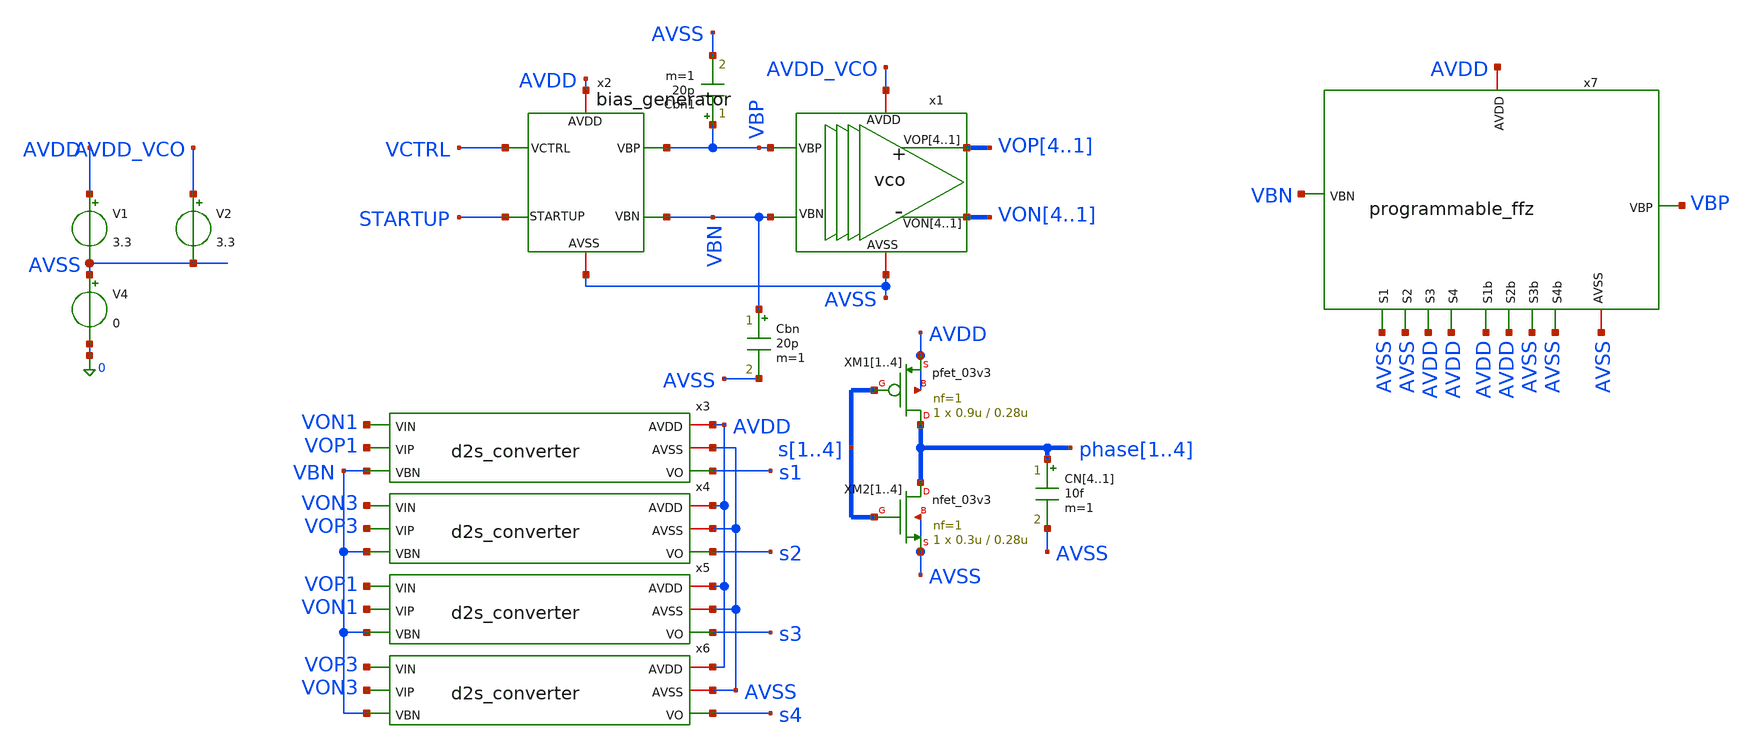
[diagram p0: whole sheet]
** sch_path: designs/libs/tb_analog/tb_quadrature_vco/tb_quadrature_vco.sch
**.subckt tb_quadrature_vco
x1 VOP4 VOP3 VOP2 VOP1 VON4 VON3 VON2 VON1 AVDD_VCO AVSS VBP VBN vco
V1 AVDD AVSS 3.3
V4 AVSS 0 0
CN4 phase1 AVSS 10f m=1
CN3 phase2 AVSS 10f m=1
CN2 phase3 AVSS 10f m=1
CN1 phase4 AVSS 10f m=1
x2 VCTRL AVDD STARTUP AVSS VBP VBN bias_generator
Cbn VBN AVSS 20p m=1
x3 AVDD AVSS VON1 VOP1 VBN s1 d2s_converter
XM11 phase1 s1 AVDD AVDD pfet_03v3 L=0.28u W=0.9u nf=1 ad='int((nf+1)/2) * W/nf * 0.18u' as='int((nf+2)/2) * W/nf * 0.18u'
+ pd='2*int((nf+1)/2) * (W/nf + 0.18u)' ps='2*int((nf+2)/2) * (W/nf + 0.18u)' nrd='0.18u / W' nrs='0.18u / W'
+ sa=0 sb=0 sd=0 m=1
XM12 phase2 s2 AVDD AVDD pfet_03v3 L=0.28u W=0.9u nf=1 ad='int((nf+1)/2) * W/nf * 0.18u' as='int((nf+2)/2) * W/nf * 0.18u'
+ pd='2*int((nf+1)/2) * (W/nf + 0.18u)' ps='2*int((nf+2)/2) * (W/nf + 0.18u)' nrd='0.18u / W' nrs='0.18u / W'
+ sa=0 sb=0 sd=0 m=1
XM13 phase3 s3 AVDD AVDD pfet_03v3 L=0.28u W=0.9u nf=1 ad='int((nf+1)/2) * W/nf * 0.18u' as='int((nf+2)/2) * W/nf * 0.18u'
+ pd='2*int((nf+1)/2) * (W/nf + 0.18u)' ps='2*int((nf+2)/2) * (W/nf + 0.18u)' nrd='0.18u / W' nrs='0.18u / W'
+ sa=0 sb=0 sd=0 m=1
XM14 phase4 s4 AVDD AVDD pfet_03v3 L=0.28u W=0.9u nf=1 ad='int((nf+1)/2) * W/nf * 0.18u' as='int((nf+2)/2) * W/nf * 0.18u'
+ pd='2*int((nf+1)/2) * (W/nf + 0.18u)' ps='2*int((nf+2)/2) * (W/nf + 0.18u)' nrd='0.18u / W' nrs='0.18u / W'
+ sa=0 sb=0 sd=0 m=1
XM21 phase1 s1 AVSS AVSS nfet_03v3 L=0.28u W=0.3u nf=1 ad='int((nf+1)/2) * W/nf * 0.18u' as='int((nf+2)/2) * W/nf * 0.18u'
+ pd='2*int((nf+1)/2) * (W/nf + 0.18u)' ps='2*int((nf+2)/2) * (W/nf + 0.18u)' nrd='0.18u / W' nrs='0.18u / W'
+ sa=0 sb=0 sd=0 m=1
XM22 phase2 s2 AVSS AVSS nfet_03v3 L=0.28u W=0.3u nf=1 ad='int((nf+1)/2) * W/nf * 0.18u' as='int((nf+2)/2) * W/nf * 0.18u'
+ pd='2*int((nf+1)/2) * (W/nf + 0.18u)' ps='2*int((nf+2)/2) * (W/nf + 0.18u)' nrd='0.18u / W' nrs='0.18u / W'
+ sa=0 sb=0 sd=0 m=1
XM23 phase3 s3 AVSS AVSS nfet_03v3 L=0.28u W=0.3u nf=1 ad='int((nf+1)/2) * W/nf * 0.18u' as='int((nf+2)/2) * W/nf * 0.18u'
+ pd='2*int((nf+1)/2) * (W/nf + 0.18u)' ps='2*int((nf+2)/2) * (W/nf + 0.18u)' nrd='0.18u / W' nrs='0.18u / W'
+ sa=0 sb=0 sd=0 m=1
XM24 phase4 s4 AVSS AVSS nfet_03v3 L=0.28u W=0.3u nf=1 ad='int((nf+1)/2) * W/nf * 0.18u' as='int((nf+2)/2) * W/nf * 0.18u'
+ pd='2*int((nf+1)/2) * (W/nf + 0.18u)' ps='2*int((nf+2)/2) * (W/nf + 0.18u)' nrd='0.18u / W' nrs='0.18u / W'
+ sa=0 sb=0 sd=0 m=1
x4 AVDD AVSS VON3 VOP3 VBN s2 d2s_converter
x5 AVDD AVSS VOP1 VON1 VBN s3 d2s_converter
x6 AVDD AVSS VOP3 VON3 VBN s4 d2s_converter
V2 AVDD_VCO AVSS 3.3
Cbn1 VBP AVSS 20p m=1
x7 VBP AVSS AVDD VBN AVDD AVSS AVDD AVSS AVSS AVDD AVSS AVDD programmable_ffz
**** begin user architecture code


.param Vin=0 Vcm=2.5
.ic v(vop1)=3.3 v(von1)=0 v(startup)=0 v(vbp)=0
.param t1=1u t2=2u t3=3u t4=4u t5=5u t6=6u t7=10u t8=100u t9=1m tr=10n

.param d0=0 d1=0.35 d2=0.825 d3=1.2375 d4=1.65 d5=2.0625 d6=2.475 d7=2.6 d8=2.75

vs startup 0 pulse(0 1 100n 10n 10n 100n 100m)
vctrl vctrl 0 pwl(0 d0  t1 d0 't1+tr' d1 t2 d1 't2+tr' d2 t3 d2 't3+tr' d3 t4 d3 't4+tr' d4 t5 d4 't5+tr'
+ d5 t6 d5 't6+tr' d6 t7 d6 't7+tr' d7 t8 d7 't8+tr' d8 t9 d8 't9+tr' d0 R 0)

*vctrl vctrl 0 1

.control
set wr_singlescale
set wr_vecnames

save v(phase1) v(phase2) v(phase3) v(phase4) v(vctrl) v(vbp) v(vbn)

OP
show all

tran 1n 1.5m
*tran 10p 10u 0 1p
*DC V5 -1 1 0.01

*let sum = v(VOP1) + v(VON1)
*let diff = v(VOP1) - v(VON1)
*let gain = deriv(diff)
*let vcm = AVG(sum/2)


*meas tran vmax MAX v(VOP1) FROM=10n TO=20n
*meas tran vmin MIN v(VOP1) FROM=10n TO=20n
*let vswing = vmax-vmin

*meas tran I_tail_avg1 AVG i(v.x1.x1.vmeas) FROM=1.01u TO=2u
*meas tran I_tail_avg2 AVG i(v.x1.x1.vmeas) FROM=2.01u TO=3u
*meas tran I_tail_avg3 AVG i(v.x1.x1.vmeas) FROM=3.01u TO=4u
*meas tran I_tail_avg4 AVG i(v.x1.x1.vmeas) FROM=4.01u TO=5u
*meas tran I_tail_avg5 AVG i(v.x1.x1.vmeas) FROM=5.01u TO=6u
*meas tran I_tail_avg6 AVG i(v.x1.x1.vmeas) FROM=6.01u TO=10u
*meas tran I_tail_avg7 AVG i(v.x1.x1.vmeas) FROM=10.01u TO=100u
*meas tran I_tail_avg8 AVG i(v.x1.x1.vmeas) FROM=100.01u TO=1m

*meas tran I_VCO1 AVG i(V2) FROM=1.01u TO=2u
*meas tran I_VCO2 AVG i(V2) FROM=2.01u TO=3u
*meas tran I_VCO3 AVG i(V2) FROM=3.01u TO=4u
*meas tran I_VCO4 AVG i(V2) FROM=4.01u TO=5u
*meas tran I_VCO5 AVG i(V2) FROM=5.01u TO=6u
*meas tran I_VCO6 AVG i(V2) FROM=6.01u TO=10u
*meas tran I_VCO7 AVG i(V2) FROM=10.01u TO=100u
*meas tran I_VCO8 AVG i(V2) FROM=100.01u TO=1m

remzerovec

write tb_quadrature_vco.raw
*wrdata /foss/designs/synchronos-chipathon-2026/designs/libs/scripts/sim_data/tb_quadrature_vco.txt
*+ tran.all
.endc



.include $::180MCU_MODELS/design.ngspice
.lib $::180MCU_MODELS/sm141064.ngspice typical
*.lib $::180MCU_MODELS/sm141064.ngspice SS
*.lib $::180MCU_MODELS/sm141064.ngspice FF
*.lib $::180MCU_MODELS/sm141064.ngspice SF
*.lib $::180MCU_MODELS/sm141064.ngspice FS

**** end user architecture code
**.ends

* expanding   symbol:  libs/core_analog/vco/vco.sym # of pins=6
** sym_path: designs/libs/core_analog/vco/vco.sym
** sch_path: designs/libs/core_analog/vco/vco.sch
.subckt vco VOP4 VOP3 VOP2 VOP1 VON4 VON3 VON2 VON1 AVDD AVSS VBP VBN
*.opin VOP1,VOP2,VOP3,VOP4
*.opin VON1,VON2,VON3,VON4
*.ipin VBP
*.ipin VBN
*.iopin AVDD
*.iopin AVSS
x1 VOP1 AVDD VOP4 VON4 VON1 AVSS VBP VBN delay_stage
x2 VOP2 AVDD VON1 VOP1 VON2 AVSS VBP VBN delay_stage
x3 VOP3 AVDD VON2 VOP2 VON3 AVSS VBP VBN delay_stage
x4 VOP4 AVDD VON3 VOP3 VON4 AVSS VBP VBN delay_stage
.ends


* expanding   symbol:  libs/core_analog/bias_generator/bias_generator.sym # of pins=6
** sym_path: designs/libs/core_analog/bias_generator/bias_generator.sym
** sch_path: designs/libs/core_analog/bias_generator/bias_generator.sch
.subckt bias_generator VCTRL AVDD STARTUP AVSS VBP VBN
*.ipin VCTRL
*.ipin STARTUP
*.iopin AVDD
*.iopin AVSS
*.opin VBP
*.opin VBN
x1 VBN AVDD net2 VCTRL AVSS net1 ota_5t
Vmeas net6 net3 0
.save i(vmeas)
Vmeas1 net7 net5 0
.save i(vmeas1)
Vmeas2 net8 net4 0
.save i(vmeas2)
XM1 net1 net1 AVDD AVDD pfet_03v3 L=0.5u W=16.8u nf=1 ad='int((nf+1)/2) * W/nf * 0.18u' as='int((nf+2)/2) * W/nf * 0.18u'
+ pd='2*int((nf+1)/2) * (W/nf + 0.18u)' ps='2*int((nf+2)/2) * (W/nf + 0.18u)' nrd='0.18u / W' nrs='0.18u / W'
+ sa=0 sb=0 sd=0 m=16
XM8 net2 AVDD net7 AVSS nfet_03v3 L=0.5u W=2.08u nf=1 ad='int((nf+1)/2) * W/nf * 0.18u' as='int((nf+2)/2) * W/nf * 0.18u'
+ pd='2*int((nf+1)/2) * (W/nf + 0.18u)' ps='2*int((nf+2)/2) * (W/nf + 0.18u)' nrd='0.18u / W' nrs='0.18u / W'
+ sa=0 sb=0 sd=0 m=8
XM9 VBP AVDD net8 AVSS nfet_03v3 L=0.5u W=2.08u nf=1 ad='int((nf+1)/2) * W/nf * 0.18u' as='int((nf+2)/2) * W/nf * 0.18u'
+ pd='2*int((nf+1)/2) * (W/nf + 0.18u)' ps='2*int((nf+2)/2) * (W/nf + 0.18u)' nrd='0.18u / W' nrs='0.18u / W'
+ sa=0 sb=0 sd=0 m=56
XM11 net1 AVDD net6 AVSS nfet_03v3 L=0.5u W=2.08u nf=1 ad='int((nf+1)/2) * W/nf * 0.18u' as='int((nf+2)/2) * W/nf * 0.18u'
+ pd='2*int((nf+1)/2) * (W/nf + 0.18u)' ps='2*int((nf+2)/2) * (W/nf + 0.18u)' nrd='0.18u / W' nrs='0.18u / W'
+ sa=0 sb=0 sd=0 m=8
XM12 net4 VBN AVSS AVSS nfet_03v3 L=0.5u W=11.25u nf=1 ad='int((nf+1)/2) * W/nf * 0.18u' as='int((nf+2)/2) * W/nf * 0.18u'
+ pd='2*int((nf+1)/2) * (W/nf + 0.18u)' ps='2*int((nf+2)/2) * (W/nf + 0.18u)' nrd='0.18u / W' nrs='0.18u / W'
+ sa=0 sb=0 sd=0 m=56
XM3 net5 VBN AVSS AVSS nfet_03v3 L=0.5u W=11.25u nf=1 ad='int((nf+1)/2) * W/nf * 0.18u' as='int((nf+2)/2) * W/nf * 0.18u'
+ pd='2*int((nf+1)/2) * (W/nf + 0.18u)' ps='2*int((nf+2)/2) * (W/nf + 0.18u)' nrd='0.18u / W' nrs='0.18u / W'
+ sa=0 sb=0 sd=0 m=8
XM4 net3 VBN AVSS AVSS nfet_03v3 L=0.5u W=11.25u nf=1 ad='int((nf+1)/2) * W/nf * 0.18u' as='int((nf+2)/2) * W/nf * 0.18u'
+ pd='2*int((nf+1)/2) * (W/nf + 0.18u)' ps='2*int((nf+2)/2) * (W/nf + 0.18u)' nrd='0.18u / W' nrs='0.18u / W'
+ sa=0 sb=0 sd=0 m=8
XM10 net3 STARTUP AVSS AVSS nfet_03v3 L=0.5u W=11.25u nf=1 ad='int((nf+1)/2) * W/nf * 0.18u' as='int((nf+2)/2) * W/nf * 0.18u'
+ pd='2*int((nf+1)/2) * (W/nf + 0.18u)' ps='2*int((nf+2)/2) * (W/nf + 0.18u)' nrd='0.18u / W' nrs='0.18u / W'
+ sa=0 sb=0 sd=0 m=8
XM2 net2 VCTRL AVDD AVDD pfet_03v3 L=1.5u W=1.1u nf=1 ad='int((nf+1)/2) * W/nf * 0.18u' as='int((nf+2)/2) * W/nf * 0.18u'
+ pd='2*int((nf+1)/2) * (W/nf + 0.18u)' ps='2*int((nf+2)/2) * (W/nf + 0.18u)' nrd='0.18u / W' nrs='0.18u / W'
+ sa=0 sb=0 sd=0 m=8
XM5 net2 net2 AVDD AVDD pfet_03v3 L=1.5u W=1.1u nf=1 ad='int((nf+1)/2) * W/nf * 0.18u' as='int((nf+2)/2) * W/nf * 0.18u'
+ pd='2*int((nf+1)/2) * (W/nf + 0.18u)' ps='2*int((nf+2)/2) * (W/nf + 0.18u)' nrd='0.18u / W' nrs='0.18u / W'
+ sa=0 sb=0 sd=0 m=8
XM6 VBP VBP AVDD AVDD pfet_03v3 L=1.5u W=1.1u nf=1 ad='int((nf+1)/2) * W/nf * 0.18u' as='int((nf+2)/2) * W/nf * 0.18u'
+ pd='2*int((nf+1)/2) * (W/nf + 0.18u)' ps='2*int((nf+2)/2) * (W/nf + 0.18u)' nrd='0.18u / W' nrs='0.18u / W'
+ sa=0 sb=0 sd=0 m=56
XM7 VBP VBP AVDD AVDD pfet_03v3 L=1.5u W=1.1u nf=1 ad='int((nf+1)/2) * W/nf * 0.18u' as='int((nf+2)/2) * W/nf * 0.18u'
+ pd='2*int((nf+1)/2) * (W/nf + 0.18u)' ps='2*int((nf+2)/2) * (W/nf + 0.18u)' nrd='0.18u / W' nrs='0.18u / W'
+ sa=0 sb=0 sd=0 m=56
.ends


* expanding   symbol:  libs/core_analog/d2s_converter/d2s_converter.sym # of pins=6
** sym_path: designs/libs/core_analog/d2s_converter/d2s_converter.sym
** sch_path: designs/libs/core_analog/d2s_converter/d2s_converter.sch
.subckt d2s_converter AVDD AVSS VIN VIP VBN VO
*.iopin AVDD
*.iopin AVSS
*.ipin VIN
*.ipin VIP
*.opin VO
*.ipin VBN
XM2 VOPB VIN i1 AVSS nfet_03v3 L=0.3u W=1.9u nf=1 ad='int((nf+1)/2) * W/nf * 0.18u' as='int((nf+2)/2) * W/nf * 0.18u'
+ pd='2*int((nf+1)/2) * (W/nf + 0.18u)' ps='2*int((nf+2)/2) * (W/nf + 0.18u)' nrd='0.18u / W' nrs='0.18u / W'
+ sa=0 sb=0 sd=0 m=4
XM4 VOPB VOPB AVDD AVDD pfet_03v3 L=0.3u W=1.4u nf=1 ad='int((nf+1)/2) * W/nf * 0.18u' as='int((nf+2)/2) * W/nf * 0.18u'
+ pd='2*int((nf+1)/2) * (W/nf + 0.18u)' ps='2*int((nf+2)/2) * (W/nf + 0.18u)' nrd='0.18u / W' nrs='0.18u / W'
+ sa=0 sb=0 sd=0 m=4
XM11 VOB VOB AVSS AVSS nfet_03v3 L=0.3u W=1.5u nf=1 ad='int((nf+1)/2) * W/nf * 0.18u' as='int((nf+2)/2) * W/nf * 0.18u'
+ pd='2*int((nf+1)/2) * (W/nf + 0.18u)' ps='2*int((nf+2)/2) * (W/nf + 0.18u)' nrd='0.18u / W' nrs='0.18u / W'
+ sa=0 sb=0 sd=0 m=4
XM13 VOB VOP AVDD AVDD pfet_03v3 L=0.3u W=2u nf=1 ad='int((nf+1)/2) * W/nf * 0.18u' as='int((nf+2)/2) * W/nf * 0.18u'
+ pd='2*int((nf+1)/2) * (W/nf + 0.18u)' ps='2*int((nf+2)/2) * (W/nf + 0.18u)' nrd='0.18u / W' nrs='0.18u / W'
+ sa=0 sb=0 sd=0 m=4
XM3 VOP VIP i1 AVSS nfet_03v3 L=0.3u W=1.9u nf=1 ad='int((nf+1)/2) * W/nf * 0.18u' as='int((nf+2)/2) * W/nf * 0.18u'
+ pd='2*int((nf+1)/2) * (W/nf + 0.18u)' ps='2*int((nf+2)/2) * (W/nf + 0.18u)' nrd='0.18u / W' nrs='0.18u / W'
+ sa=0 sb=0 sd=0 m=4
XM5 VOP VOPB AVDD AVDD pfet_03v3 L=0.3u W=1.4u nf=1 ad='int((nf+1)/2) * W/nf * 0.18u' as='int((nf+2)/2) * W/nf * 0.18u'
+ pd='2*int((nf+1)/2) * (W/nf + 0.18u)' ps='2*int((nf+2)/2) * (W/nf + 0.18u)' nrd='0.18u / W' nrs='0.18u / W'
+ sa=0 sb=0 sd=0 m=4
XM7 VONB VIP i2 AVSS nfet_03v3 L=0.3u W=1.9u nf=1 ad='int((nf+1)/2) * W/nf * 0.18u' as='int((nf+2)/2) * W/nf * 0.18u'
+ pd='2*int((nf+1)/2) * (W/nf + 0.18u)' ps='2*int((nf+2)/2) * (W/nf + 0.18u)' nrd='0.18u / W' nrs='0.18u / W'
+ sa=0 sb=0 sd=0 m=4
XM8 VONB VONB AVDD AVDD pfet_03v3 L=0.3u W=1.4u nf=1 ad='int((nf+1)/2) * W/nf * 0.18u' as='int((nf+2)/2) * W/nf * 0.18u'
+ pd='2*int((nf+1)/2) * (W/nf + 0.18u)' ps='2*int((nf+2)/2) * (W/nf + 0.18u)' nrd='0.18u / W' nrs='0.18u / W'
+ sa=0 sb=0 sd=0 m=4
XM9 VON VIN i2 AVSS nfet_03v3 L=0.3u W=1.9u nf=1 ad='int((nf+1)/2) * W/nf * 0.18u' as='int((nf+2)/2) * W/nf * 0.18u'
+ pd='2*int((nf+1)/2) * (W/nf + 0.18u)' ps='2*int((nf+2)/2) * (W/nf + 0.18u)' nrd='0.18u / W' nrs='0.18u / W'
+ sa=0 sb=0 sd=0 m=4
XM10 VON VONB AVDD AVDD pfet_03v3 L=0.3u W=1.4u nf=1 ad='int((nf+1)/2) * W/nf * 0.18u' as='int((nf+2)/2) * W/nf * 0.18u'
+ pd='2*int((nf+1)/2) * (W/nf + 0.18u)' ps='2*int((nf+2)/2) * (W/nf + 0.18u)' nrd='0.18u / W' nrs='0.18u / W'
+ sa=0 sb=0 sd=0 m=4
XM14 VO VON AVDD AVDD pfet_03v3 L=0.3u W=2u nf=1 ad='int((nf+1)/2) * W/nf * 0.18u' as='int((nf+2)/2) * W/nf * 0.18u'
+ pd='2*int((nf+1)/2) * (W/nf + 0.18u)' ps='2*int((nf+2)/2) * (W/nf + 0.18u)' nrd='0.18u / W' nrs='0.18u / W'
+ sa=0 sb=0 sd=0 m=4
XM12 VO VOB AVSS AVSS nfet_03v3 L=0.3u W=1.5u nf=1 ad='int((nf+1)/2) * W/nf * 0.18u' as='int((nf+2)/2) * W/nf * 0.18u'
+ pd='2*int((nf+1)/2) * (W/nf + 0.18u)' ps='2*int((nf+2)/2) * (W/nf + 0.18u)' nrd='0.18u / W' nrs='0.18u / W'
+ sa=0 sb=0 sd=0 m=4
XM1 i1 VBN AVSS AVSS nfet_03v3 L=0.5u W=11.25u nf=1 ad='int((nf+1)/2) * W/nf * 0.18u' as='int((nf+2)/2) * W/nf * 0.18u'
+ pd='2*int((nf+1)/2) * (W/nf + 0.18u)' ps='2*int((nf+2)/2) * (W/nf + 0.18u)' nrd='0.18u / W' nrs='0.18u / W'
+ sa=0 sb=0 sd=0 m=4
XM6 i2 VBN AVSS AVSS nfet_03v3 L=0.5u W=11.25u nf=1 ad='int((nf+1)/2) * W/nf * 0.18u' as='int((nf+2)/2) * W/nf * 0.18u'
+ pd='2*int((nf+1)/2) * (W/nf + 0.18u)' ps='2*int((nf+2)/2) * (W/nf + 0.18u)' nrd='0.18u / W' nrs='0.18u / W'
+ sa=0 sb=0 sd=0 m=4
.ends


* expanding   symbol:  libs/core_analog/programmable_ffz/programmable_ffz.sym # of pins=12
** sym_path: designs/libs/core_analog/programmable_ffz/programmable_ffz.sym
** sch_path: designs/libs/core_analog/programmable_ffz/programmable_ffz.sch
.subckt programmable_ffz VBP AVSS AVDD VBN S1b S1 S2b S2 S3b S3 S4b S4
*.ipin VBN
*.ipin S1b
*.ipin S1
*.ipin S2b
*.ipin S2
*.ipin S3b
*.ipin S3
*.ipin S4b
*.ipin S4
*.iopin AVSS
*.iopin AVDD
*.opin VBP
x2 VBN AVSS S1 VBN1 S1b AVDD transmission_gate
x3 VBN AVSS S2 VBN2 S2b AVDD transmission_gate
x4 VBN AVSS S3 VBN3 S3b AVDD transmission_gate
x5 VBN AVSS S4 VBN4 S4b AVDD transmission_gate
x1 AVDD VBP VBN AVSS AVSS feed_forward_zero
x6 AVDD net1 VBN1 S1b AVSS feed_forward_zero
x71 AVDD net2 VBN2 S2b AVSS feed_forward_zero
x72 AVDD net2 VBN2 S2b AVSS feed_forward_zero
x11 AVDD net3 VBN3 S3b AVSS feed_forward_zero
x12 AVDD net3 VBN3 S3b AVSS feed_forward_zero
x13 AVDD net3 VBN3 S3b AVSS feed_forward_zero
x14 AVDD net3 VBN3 S3b AVSS feed_forward_zero
x21 AVDD net4 VBN4 S4b AVSS feed_forward_zero
x22 AVDD net4 VBN4 S4b AVSS feed_forward_zero
x23 AVDD net4 VBN4 S4b AVSS feed_forward_zero
x24 AVDD net4 VBN4 S4b AVSS feed_forward_zero
x25 AVDD net4 VBN4 S4b AVSS feed_forward_zero
x26 AVDD net4 VBN4 S4b AVSS feed_forward_zero
x27 AVDD net4 VBN4 S4b AVSS feed_forward_zero
x28 AVDD net4 VBN4 S4b AVSS feed_forward_zero
x7 net1 AVSS S1 VBP S1b AVDD transmission_gate
x8 net2 AVSS S2 VBP S2b AVDD transmission_gate
x9 net3 AVSS S3 VBP S3b AVDD transmission_gate
x10 net4 AVSS S4 VBP S4b AVDD transmission_gate
.ends


* expanding   symbol:  libs/core_analog/delay_stage/delay_stage.sym # of pins=8
** sym_path: designs/libs/core_analog/delay_stage/delay_stage.sym
** sch_path: designs/libs/core_analog/delay_stage/delay_stage.sch
.subckt delay_stage VOP AVDD VIP VIN VON AVSS VBP VBN
*.ipin VIP
*.ipin VIN
*.opin VOP
*.opin VON
*.iopin AVDD
*.iopin AVSS
*.ipin VBP
*.ipin VBN
XM5 VON VIP net1 AVSS nfet_03v3 L=0.5u W=2.08u nf=1 ad='int((nf+1)/2) * W/nf * 0.18u' as='int((nf+2)/2) * W/nf * 0.18u'
+ pd='2*int((nf+1)/2) * (W/nf + 0.18u)' ps='2*int((nf+2)/2) * (W/nf + 0.18u)' nrd='0.18u / W' nrs='0.18u / W'
+ sa=0 sb=0 sd=0 m=8
XM2 VON VON AVDD AVDD pfet_03v3 L=1.5u W=1.1u nf=1 ad='int((nf+1)/2) * W/nf * 0.18u' as='int((nf+2)/2) * W/nf * 0.18u'
+ pd='2*int((nf+1)/2) * (W/nf + 0.18u)' ps='2*int((nf+2)/2) * (W/nf + 0.18u)' nrd='0.18u / W' nrs='0.18u / W'
+ sa=0 sb=0 sd=0 m=8
XM6 VOP VIN net1 AVSS nfet_03v3 L=0.5u W=2.08u nf=1 ad='int((nf+1)/2) * W/nf * 0.18u' as='int((nf+2)/2) * W/nf * 0.18u'
+ pd='2*int((nf+1)/2) * (W/nf + 0.18u)' ps='2*int((nf+2)/2) * (W/nf + 0.18u)' nrd='0.18u / W' nrs='0.18u / W'
+ sa=0 sb=0 sd=0 m=8
XM1 VON VBP AVDD AVDD pfet_03v3 L=1.5u W=1.1u nf=1 ad='int((nf+1)/2) * W/nf * 0.18u' as='int((nf+2)/2) * W/nf * 0.18u'
+ pd='2*int((nf+1)/2) * (W/nf + 0.18u)' ps='2*int((nf+2)/2) * (W/nf + 0.18u)' nrd='0.18u / W' nrs='0.18u / W'
+ sa=0 sb=0 sd=0 m=8
XM3 VOP VBP AVDD AVDD pfet_03v3 L=1.5u W=1.1u nf=1 ad='int((nf+1)/2) * W/nf * 0.18u' as='int((nf+2)/2) * W/nf * 0.18u'
+ pd='2*int((nf+1)/2) * (W/nf + 0.18u)' ps='2*int((nf+2)/2) * (W/nf + 0.18u)' nrd='0.18u / W' nrs='0.18u / W'
+ sa=0 sb=0 sd=0 m=8
XM4 VOP VOP AVDD AVDD pfet_03v3 L=1.5u W=1.1u nf=1 ad='int((nf+1)/2) * W/nf * 0.18u' as='int((nf+2)/2) * W/nf * 0.18u'
+ pd='2*int((nf+1)/2) * (W/nf + 0.18u)' ps='2*int((nf+2)/2) * (W/nf + 0.18u)' nrd='0.18u / W' nrs='0.18u / W'
+ sa=0 sb=0 sd=0 m=8
XM8 net1 VBN AVSS AVSS nfet_03v3 L=0.5u W=11.25u nf=1 ad='int((nf+1)/2) * W/nf * 0.18u' as='int((nf+2)/2) * W/nf * 0.18u'
+ pd='2*int((nf+1)/2) * (W/nf + 0.18u)' ps='2*int((nf+2)/2) * (W/nf + 0.18u)' nrd='0.18u / W' nrs='0.18u / W'
+ sa=0 sb=0 sd=0 m=8
.ends


* expanding   symbol:  libs/core_analog/ota_5t/ota_5t.sym # of pins=6
** sym_path: designs/libs/core_analog/ota_5t/ota_5t.sym
** sch_path: designs/libs/core_analog/ota_5t/ota_5t.sch
.subckt ota_5t VO AVDD VI+ VI- AVSS VB
*.ipin VI+
*.ipin VI-
*.ipin VB
*.iopin AVDD
*.iopin AVSS
*.opin VO
XM1 VO VI- net2 AVDD pfet_03v3 L=0.5u W=6.55u nf=1 ad='int((nf+1)/2) * W/nf * 0.18u' as='int((nf+2)/2) * W/nf * 0.18u'
+ pd='2*int((nf+1)/2) * (W/nf + 0.18u)' ps='2*int((nf+2)/2) * (W/nf + 0.18u)' nrd='0.18u / W' nrs='0.18u / W'
+ sa=0 sb=0 sd=0 m=8
XM4 VO net1 AVSS AVSS nfet_03v3 L=0.5u W=4.8u nf=1 ad='int((nf+1)/2) * W/nf * 0.18u' as='int((nf+2)/2) * W/nf * 0.18u'
+ pd='2*int((nf+1)/2) * (W/nf + 0.18u)' ps='2*int((nf+2)/2) * (W/nf + 0.18u)' nrd='0.18u / W' nrs='0.18u / W'
+ sa=0 sb=0 sd=0 m=4
XM3 net2 VB net3 AVDD pfet_03v3 L=0.5u W=8.3u nf=1 ad='int((nf+1)/2) * W/nf * 0.18u' as='int((nf+2)/2) * W/nf * 0.18u'
+ pd='2*int((nf+1)/2) * (W/nf + 0.18u)' ps='2*int((nf+2)/2) * (W/nf + 0.18u)' nrd='0.18u / W' nrs='0.18u / W'
+ sa=0 sb=0 sd=0 m=16
XM2 net1 VI+ net2 AVDD pfet_03v3 L=0.5u W=6.55u nf=1 ad='int((nf+1)/2) * W/nf * 0.18u' as='int((nf+2)/2) * W/nf * 0.18u'
+ pd='2*int((nf+1)/2) * (W/nf + 0.18u)' ps='2*int((nf+2)/2) * (W/nf + 0.18u)' nrd='0.18u / W' nrs='0.18u / W'
+ sa=0 sb=0 sd=0 m=8
XM5 net1 net1 AVSS AVSS nfet_03v3 L=0.5u W=4.8u nf=1 ad='int((nf+1)/2) * W/nf * 0.18u' as='int((nf+2)/2) * W/nf * 0.18u'
+ pd='2*int((nf+1)/2) * (W/nf + 0.18u)' ps='2*int((nf+2)/2) * (W/nf + 0.18u)' nrd='0.18u / W' nrs='0.18u / W'
+ sa=0 sb=0 sd=0 m=4
Vmeas AVDD net3 0
.save i(vmeas)
.ends


* expanding   symbol:  libs/core_analog/transmission_gate/transmission_gate.sym # of pins=6
** sym_path: designs/libs/core_analog/transmission_gate/transmission_gate.sym
** sch_path: designs/libs/core_analog/transmission_gate/transmission_gate.sch
.subckt transmission_gate ind vss clkn ins clkp vdd
*.iopin ind
*.iopin ins
*.iopin clkn
*.iopin clkp
*.iopin vdd
*.iopin vss
XM1 ind clkp ins vdd pfet_03v3 L=0.5u W=3.0u nf=1 ad='int((nf+1)/2) * W/nf * 0.18u' as='int((nf+2)/2) * W/nf * 0.18u'
+ pd='2*int((nf+1)/2) * (W/nf + 0.18u)' ps='2*int((nf+2)/2) * (W/nf + 0.18u)' nrd='0.18u / W' nrs='0.18u / W'
+ sa=0 sb=0 sd=0 m=1
XM2 ind clkn ins vss nfet_03v3 L=0.5u W=1.0u nf=1 ad='int((nf+1)/2) * W/nf * 0.18u' as='int((nf+2)/2) * W/nf * 0.18u'
+ pd='2*int((nf+1)/2) * (W/nf + 0.18u)' ps='2*int((nf+2)/2) * (W/nf + 0.18u)' nrd='0.18u / W' nrs='0.18u / W'
+ sa=0 sb=0 sd=0 m=1
.ends


* expanding   symbol:  libs/core_analog/feed_forward_zero/feed_forward_zero.sym # of pins=5
** sym_path: designs/libs/core_analog/feed_forward_zero/feed_forward_zero.sym
** sch_path: designs/libs/core_analog/feed_forward_zero/feed_forward_zero.sch
.subckt feed_forward_zero AVDD VBP VBN S AVSS
*.opin VBP
*.iopin AVDD
*.iopin AVSS
*.ipin VBN
*.ipin S
XM1 VBP VBP AVDD AVDD pfet_03v3 L=1.5u W=1.1u nf=1 ad='int((nf+1)/2) * W/nf * 0.18u' as='int((nf+2)/2) * W/nf * 0.18u'
+ pd='2*int((nf+1)/2) * (W/nf + 0.18u)' ps='2*int((nf+2)/2) * (W/nf + 0.18u)' nrd='0.18u / W' nrs='0.18u / W'
+ sa=0 sb=0 sd=0 m=2
XM2 VBP VBP AVDD AVDD pfet_03v3 L=1.5u W=1.1u nf=1 ad='int((nf+1)/2) * W/nf * 0.18u' as='int((nf+2)/2) * W/nf * 0.18u'
+ pd='2*int((nf+1)/2) * (W/nf + 0.18u)' ps='2*int((nf+2)/2) * (W/nf + 0.18u)' nrd='0.18u / W' nrs='0.18u / W'
+ sa=0 sb=0 sd=0 m=2
XM3 VBP AVDD net1 AVSS nfet_03v3 L=0.5u W=2.08u nf=1 ad='int((nf+1)/2) * W/nf * 0.18u' as='int((nf+2)/2) * W/nf * 0.18u'
+ pd='2*int((nf+1)/2) * (W/nf + 0.18u)' ps='2*int((nf+2)/2) * (W/nf + 0.18u)' nrd='0.18u / W' nrs='0.18u / W'
+ sa=0 sb=0 sd=0 m=2
XM4 net1 VBN AVSS AVSS nfet_03v3 L=0.5u W=11.25u nf=1 ad='int((nf+1)/2) * W/nf * 0.18u' as='int((nf+2)/2) * W/nf * 0.18u'
+ pd='2*int((nf+1)/2) * (W/nf + 0.18u)' ps='2*int((nf+2)/2) * (W/nf + 0.18u)' nrd='0.18u / W' nrs='0.18u / W'
+ sa=0 sb=0 sd=0 m=2
XM7 VBN S AVSS AVSS nfet_03v3 L=0.5u W=1u nf=1 ad='int((nf+1)/2) * W/nf * 0.18u' as='int((nf+2)/2) * W/nf * 0.18u'
+ pd='2*int((nf+1)/2) * (W/nf + 0.18u)' ps='2*int((nf+2)/2) * (W/nf + 0.18u)' nrd='0.18u / W' nrs='0.18u / W'
+ sa=0 sb=0 sd=0 m=1
.ends

.end
